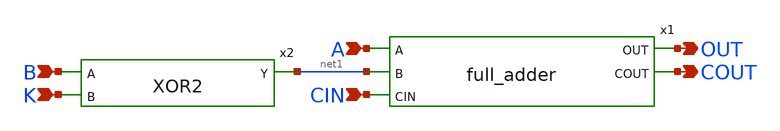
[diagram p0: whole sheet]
** sch_path: design/xschem/ADDER/full_adder_substractor.sch
**.subckt full_adder_substractor K B CIN OUT COUT A
*.ipin K
*.ipin B
*.ipin CIN
*.opin OUT
*.opin COUT
*.ipin A
x1 OUT A net1 CIN COUT VSS VDD full_adder
x2 B K net1 VSS VDD XOR2
**.ends
.end
